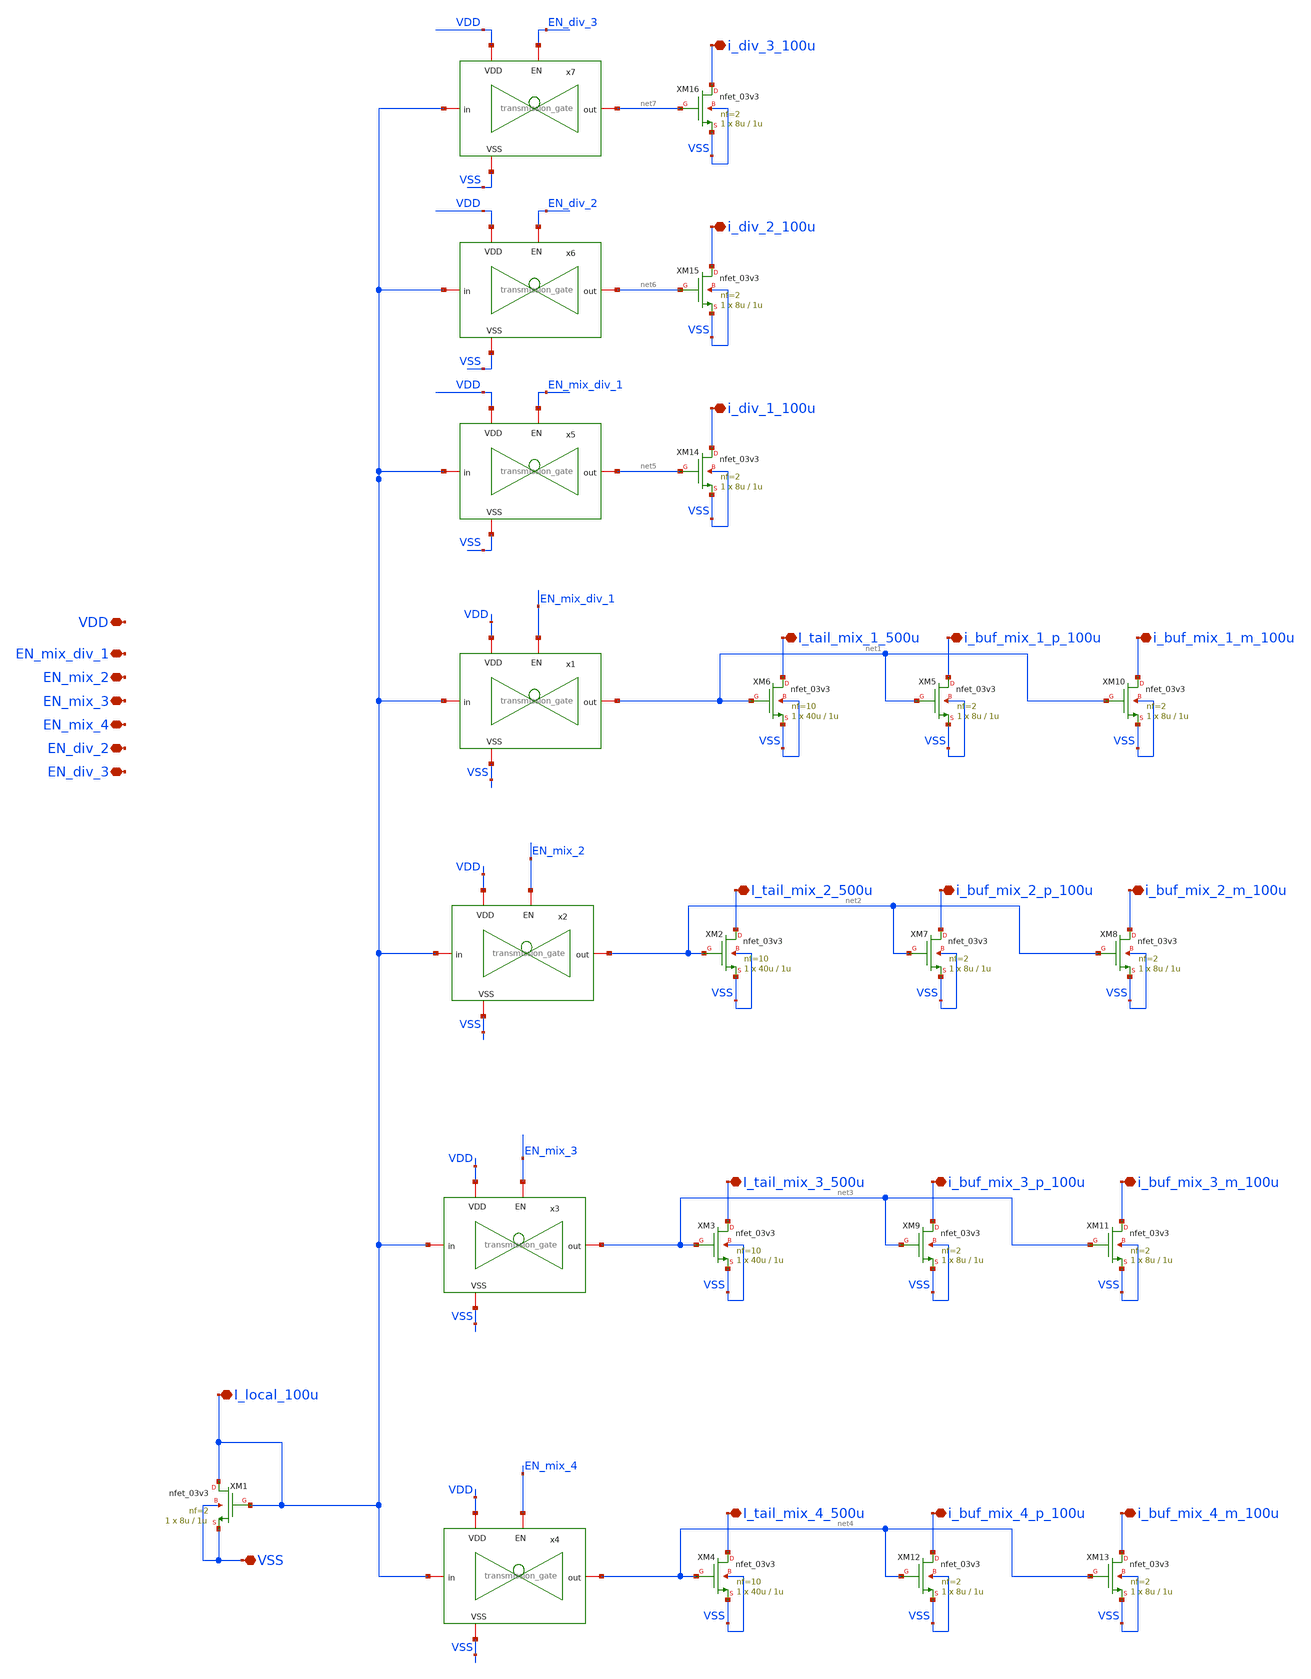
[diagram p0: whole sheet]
** sch_path: designs/mirrors/schematic/Lei_nmos_mirror.sch
**.subckt Lei_nmos_mirror I_local_100u I_tail_mix_1_500u VDD VSS EN_mix_div_1 I_tail_mix_2_500u
*+ I_tail_mix_3_500u I_tail_mix_4_500u EN_mix_2 EN_mix_3 EN_mix_4 i_buf_mix_1_p_100u i_buf_mix_1_m_100u
*+ i_buf_mix_2_p_100u i_buf_mix_2_m_100u i_buf_mix_3_p_100u i_buf_mix_3_m_100u i_buf_mix_4_p_100u i_buf_mix_4_m_100u
*+ EN_div_2 EN_div_3 i_div_1_100u i_div_2_100u i_div_3_100u
*.iopin I_local_100u
*.iopin I_tail_mix_1_500u
*.iopin VDD
*.iopin VSS
*.iopin EN_mix_div_1
*.iopin I_tail_mix_2_500u
*.iopin I_tail_mix_3_500u
*.iopin I_tail_mix_4_500u
*.iopin EN_mix_2
*.iopin EN_mix_3
*.iopin EN_mix_4
*.iopin i_buf_mix_1_p_100u
*.iopin i_buf_mix_1_m_100u
*.iopin i_buf_mix_2_p_100u
*.iopin i_buf_mix_2_m_100u
*.iopin i_buf_mix_3_p_100u
*.iopin i_buf_mix_3_m_100u
*.iopin i_buf_mix_4_p_100u
*.iopin i_buf_mix_4_m_100u
*.iopin EN_div_2
*.iopin EN_div_3
*.iopin i_div_1_100u
*.iopin i_div_2_100u
*.iopin i_div_3_100u
XM1 I_local_100u I_local_100u VSS VSS nfet_03v3 L=1u W=8u nf=2 ad='int((nf+1)/2) * W/nf * 0.18u' as='int((nf+2)/2) * W/nf * 0.18u'
+ pd='2*int((nf+1)/2) * (W/nf + 0.18u)' ps='2*int((nf+2)/2) * (W/nf + 0.18u)' nrd='0.18u / W' nrs='0.18u / W'
+ sa=0 sb=0 sd=0 m=1
XM6 I_tail_mix_1_500u net1 VSS VSS nfet_03v3 L=1u W=40u nf=10 ad='int((nf+1)/2) * W/nf * 0.18u' as='int((nf+2)/2) * W/nf * 0.18u'
+ pd='2*int((nf+1)/2) * (W/nf + 0.18u)' ps='2*int((nf+2)/2) * (W/nf + 0.18u)' nrd='0.18u / W' nrs='0.18u / W'
+ sa=0 sb=0 sd=0 m=1
x1 EN_mix_div_1 VDD I_local_100u net1 VSS transmission_gate
XM2 I_tail_mix_2_500u net2 VSS VSS nfet_03v3 L=1u W=40u nf=10 ad='int((nf+1)/2) * W/nf * 0.18u' as='int((nf+2)/2) * W/nf * 0.18u'
+ pd='2*int((nf+1)/2) * (W/nf + 0.18u)' ps='2*int((nf+2)/2) * (W/nf + 0.18u)' nrd='0.18u / W' nrs='0.18u / W'
+ sa=0 sb=0 sd=0 m=1
XM3 I_tail_mix_3_500u net3 VSS VSS nfet_03v3 L=1u W=40u nf=10 ad='int((nf+1)/2) * W/nf * 0.18u' as='int((nf+2)/2) * W/nf * 0.18u'
+ pd='2*int((nf+1)/2) * (W/nf + 0.18u)' ps='2*int((nf+2)/2) * (W/nf + 0.18u)' nrd='0.18u / W' nrs='0.18u / W'
+ sa=0 sb=0 sd=0 m=1
XM4 I_tail_mix_4_500u net4 VSS VSS nfet_03v3 L=1u W=40u nf=10 ad='int((nf+1)/2) * W/nf * 0.18u' as='int((nf+2)/2) * W/nf * 0.18u'
+ pd='2*int((nf+1)/2) * (W/nf + 0.18u)' ps='2*int((nf+2)/2) * (W/nf + 0.18u)' nrd='0.18u / W' nrs='0.18u / W'
+ sa=0 sb=0 sd=0 m=1
x2 EN_mix_2 VDD I_local_100u net2 VSS transmission_gate
x3 EN_mix_3 VDD I_local_100u net3 VSS transmission_gate
x4 EN_mix_4 VDD I_local_100u net4 VSS transmission_gate
XM5 i_buf_mix_1_p_100u net1 VSS VSS nfet_03v3 L=1u W=8u nf=2 ad='int((nf+1)/2) * W/nf * 0.18u' as='int((nf+2)/2) * W/nf * 0.18u'
+ pd='2*int((nf+1)/2) * (W/nf + 0.18u)' ps='2*int((nf+2)/2) * (W/nf + 0.18u)' nrd='0.18u / W' nrs='0.18u / W'
+ sa=0 sb=0 sd=0 m=1
XM10 i_buf_mix_1_m_100u net1 VSS VSS nfet_03v3 L=1u W=8u nf=2 ad='int((nf+1)/2) * W/nf * 0.18u' as='int((nf+2)/2) * W/nf * 0.18u'
+ pd='2*int((nf+1)/2) * (W/nf + 0.18u)' ps='2*int((nf+2)/2) * (W/nf + 0.18u)' nrd='0.18u / W' nrs='0.18u / W'
+ sa=0 sb=0 sd=0 m=1
XM7 i_buf_mix_2_p_100u net2 VSS VSS nfet_03v3 L=1u W=8u nf=2 ad='int((nf+1)/2) * W/nf * 0.18u' as='int((nf+2)/2) * W/nf * 0.18u'
+ pd='2*int((nf+1)/2) * (W/nf + 0.18u)' ps='2*int((nf+2)/2) * (W/nf + 0.18u)' nrd='0.18u / W' nrs='0.18u / W'
+ sa=0 sb=0 sd=0 m=1
XM8 i_buf_mix_2_m_100u net2 VSS VSS nfet_03v3 L=1u W=8u nf=2 ad='int((nf+1)/2) * W/nf * 0.18u' as='int((nf+2)/2) * W/nf * 0.18u'
+ pd='2*int((nf+1)/2) * (W/nf + 0.18u)' ps='2*int((nf+2)/2) * (W/nf + 0.18u)' nrd='0.18u / W' nrs='0.18u / W'
+ sa=0 sb=0 sd=0 m=1
XM9 i_buf_mix_3_p_100u net3 VSS VSS nfet_03v3 L=1u W=8u nf=2 ad='int((nf+1)/2) * W/nf * 0.18u' as='int((nf+2)/2) * W/nf * 0.18u'
+ pd='2*int((nf+1)/2) * (W/nf + 0.18u)' ps='2*int((nf+2)/2) * (W/nf + 0.18u)' nrd='0.18u / W' nrs='0.18u / W'
+ sa=0 sb=0 sd=0 m=1
XM11 i_buf_mix_3_m_100u net3 VSS VSS nfet_03v3 L=1u W=8u nf=2 ad='int((nf+1)/2) * W/nf * 0.18u' as='int((nf+2)/2) * W/nf * 0.18u'
+ pd='2*int((nf+1)/2) * (W/nf + 0.18u)' ps='2*int((nf+2)/2) * (W/nf + 0.18u)' nrd='0.18u / W' nrs='0.18u / W'
+ sa=0 sb=0 sd=0 m=1
XM12 i_buf_mix_4_p_100u net4 VSS VSS nfet_03v3 L=1u W=8u nf=2 ad='int((nf+1)/2) * W/nf * 0.18u' as='int((nf+2)/2) * W/nf * 0.18u'
+ pd='2*int((nf+1)/2) * (W/nf + 0.18u)' ps='2*int((nf+2)/2) * (W/nf + 0.18u)' nrd='0.18u / W' nrs='0.18u / W'
+ sa=0 sb=0 sd=0 m=1
XM13 i_buf_mix_4_m_100u net4 VSS VSS nfet_03v3 L=1u W=8u nf=2 ad='int((nf+1)/2) * W/nf * 0.18u' as='int((nf+2)/2) * W/nf * 0.18u'
+ pd='2*int((nf+1)/2) * (W/nf + 0.18u)' ps='2*int((nf+2)/2) * (W/nf + 0.18u)' nrd='0.18u / W' nrs='0.18u / W'
+ sa=0 sb=0 sd=0 m=1
x5 EN_mix_div_1 VDD I_local_100u net5 VSS transmission_gate
XM14 i_div_1_100u net5 VSS VSS nfet_03v3 L=1u W=8u nf=2 ad='int((nf+1)/2) * W/nf * 0.18u' as='int((nf+2)/2) * W/nf * 0.18u'
+ pd='2*int((nf+1)/2) * (W/nf + 0.18u)' ps='2*int((nf+2)/2) * (W/nf + 0.18u)' nrd='0.18u / W' nrs='0.18u / W'
+ sa=0 sb=0 sd=0 m=1
x6 EN_div_2 VDD I_local_100u net6 VSS transmission_gate
XM15 i_div_2_100u net6 VSS VSS nfet_03v3 L=1u W=8u nf=2 ad='int((nf+1)/2) * W/nf * 0.18u' as='int((nf+2)/2) * W/nf * 0.18u'
+ pd='2*int((nf+1)/2) * (W/nf + 0.18u)' ps='2*int((nf+2)/2) * (W/nf + 0.18u)' nrd='0.18u / W' nrs='0.18u / W'
+ sa=0 sb=0 sd=0 m=1
x7 EN_div_3 VDD I_local_100u net7 VSS transmission_gate
XM16 i_div_3_100u net7 VSS VSS nfet_03v3 L=1u W=8u nf=2 ad='int((nf+1)/2) * W/nf * 0.18u' as='int((nf+2)/2) * W/nf * 0.18u'
+ pd='2*int((nf+1)/2) * (W/nf + 0.18u)' ps='2*int((nf+2)/2) * (W/nf + 0.18u)' nrd='0.18u / W' nrs='0.18u / W'
+ sa=0 sb=0 sd=0 m=1
**.ends

* expanding   symbol:  designs/digital/schematic/transmission_gate.sym # of pins=5
** sym_path: designs/digital/schematic/transmission_gate.sym
** sch_path: designs/digital/schematic/transmission_gate.sch
.subckt transmission_gate EN VDD in out VSS
*.iopin VDD
*.iopin VSS
*.iopin in
*.iopin out
*.iopin EN
XM1 in EN_B out VDD pfet_03v3 L=0.28u W=2u nf=1 ad='int((nf+1)/2) * W/nf * 0.18u' as='int((nf+2)/2) * W/nf * 0.18u'
+ pd='2*int((nf+1)/2) * (W/nf + 0.18u)' ps='2*int((nf+2)/2) * (W/nf + 0.18u)' nrd='0.18u / W' nrs='0.18u / W'
+ sa=0 sb=0 sd=0 m=1
XM2 in EN out VSS nfet_03v3 L=0.28u W=1u nf=1 ad='int((nf+1)/2) * W/nf * 0.18u' as='int((nf+2)/2) * W/nf * 0.18u'
+ pd='2*int((nf+1)/2) * (W/nf + 0.18u)' ps='2*int((nf+2)/2) * (W/nf + 0.18u)' nrd='0.18u / W' nrs='0.18u / W'
+ sa=0 sb=0 sd=0 m=1
XM3 out EN_B VSS VSS nfet_03v3 L=0.28u W=1u nf=1 ad='int((nf+1)/2) * W/nf * 0.18u' as='int((nf+2)/2) * W/nf * 0.18u'
+ pd='2*int((nf+1)/2) * (W/nf + 0.18u)' ps='2*int((nf+2)/2) * (W/nf + 0.18u)' nrd='0.18u / W' nrs='0.18u / W'
+ sa=0 sb=0 sd=0 m=1
XM4 EN_B EN VDD VDD pfet_03v3 L=0.28u W=1u nf=1 ad='int((nf+1)/2) * W/nf * 0.18u' as='int((nf+2)/2) * W/nf * 0.18u'
+ pd='2*int((nf+1)/2) * (W/nf + 0.18u)' ps='2*int((nf+2)/2) * (W/nf + 0.18u)' nrd='0.18u / W' nrs='0.18u / W'
+ sa=0 sb=0 sd=0 m=1
XM5 EN_B EN VSS VSS nfet_03v3 L=0.28u W=1u nf=1 ad='int((nf+1)/2) * W/nf * 0.18u' as='int((nf+2)/2) * W/nf * 0.18u'
+ pd='2*int((nf+1)/2) * (W/nf + 0.18u)' ps='2*int((nf+2)/2) * (W/nf + 0.18u)' nrd='0.18u / W' nrs='0.18u / W'
+ sa=0 sb=0 sd=0 m=1
.ends

.end
